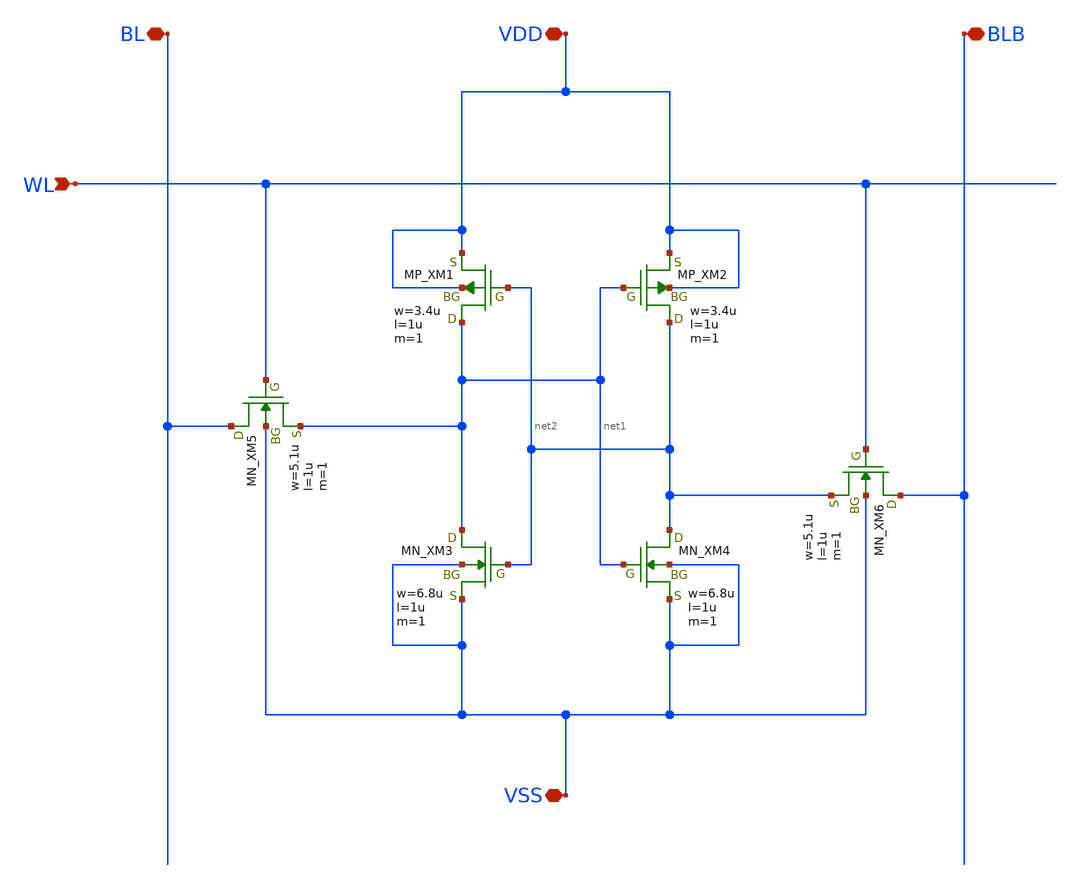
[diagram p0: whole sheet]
** sch_path: sram/sram6t_tr10.sch
**.subckt sram6t_tr10 BL BLB WL VDD VSS
*.iopin BL
*.iopin BLB
*.ipin WL
*.iopin VDD
*.iopin VSS
XXM1 net1 net2 VDD VDD PMOS w=3.4u l=1u nrd=0 nrs=0 m=1
XXM2 net2 net1 VDD VDD PMOS w=3.4u l=1u nrd=0 nrs=0 m=1
XXM4 net2 net1 VSS VSS NMOS w=6.8u l=1u nrd=0 nrs=0 m=1
XXM3 net1 net2 VSS VSS NMOS w=6.8u l=1u nrd=0 nrs=0 m=1
XXM5 BL WL net1 VSS NMOS w=5.1u l=1u nrd=0 nrs=0 m=1
XXM6 BLB WL net2 VSS NMOS w=5.1u l=1u nrd=0 nrs=0 m=1
**.ends
.end
